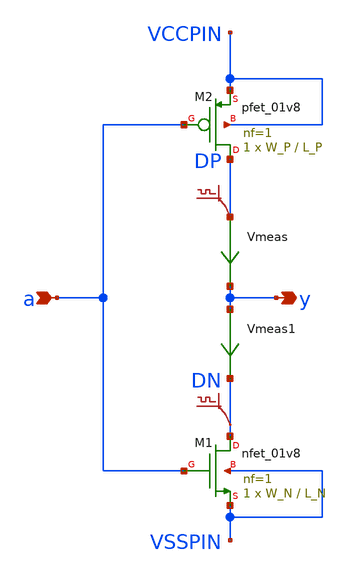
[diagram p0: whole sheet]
** sch_path: sky130A/xschem_libs/sky130_tests/not/schematic/not.sch
* Copyright 2021 Stefan Frederik Schippers
* Licensed under the Apache License, Version 2.0 (the "License");
* you may not use this file except in compliance with the License.
* You may obtain a copy of the License at
* https://www.apache.org/licenses/LICENSE-2.0
* Unless required by applicable law or agreed to in writing, software
* distributed under the License is distributed on an "AS IS" BASIS,
* WITHOUT WARRANTIES OR CONDITIONS OF ANY KIND, either express or implied.
* See the License for the specific language governing permissions and
* limitations under the License.
**.subckt not y a
*.opin y
*.ipin a
XM1 DN a VSSPIN VSSPIN sky130_fd_pr__nfet_01v8 L=L_N W=W_N nf=1 ad='int((1 + 1)/2) * W_N / 1 * 0.29'
+ as='int((1 + 2)/2) * W_N / 1 * 0.29' pd='2*int((1 + 1)/2) * (W_N / 1 + 0.29)' ps='2*int((1 + 2)/2) * (W_N / 1 + 0.29)'
+ nrd='0.29 / W_N ' nrs='0.29 / W_N ' sa=0 sb=0 sd=0 mult=1 m=1
XM2 DP a VCCPIN VCCPIN sky130_fd_pr__pfet_01v8 L=L_P W=W_P nf=1 ad='int((nf+1)/2) * W/nf * 0.29' as='int((nf+2)/2) * W/nf * 0.29'
+ pd='2*int((nf+1)/2) * (W/nf + 0.29)' ps='2*int((nf+2)/2) * (W/nf + 0.29)' nrd='0.29 / W' nrs='0.29 / W'
+ sa=0 sb=0 sd=0 mult=1 m=1
Vmeas DP y 0
.save i(vmeas)
Vmeas1 y DN 0
.save i(vmeas1)
.save v(dp)
.save v(dn)
**.ends
.end
